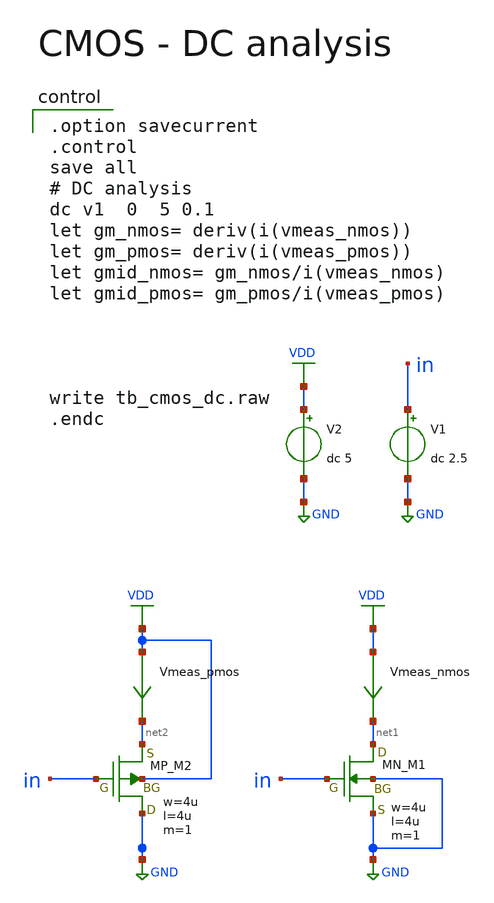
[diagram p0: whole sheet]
** sch_path: member_project/AM_Radio/Yamada3/xschem/tb_cmos_dc.sch
**.subckt tb_cmos_dc
V2 VDD GND dc 5
V1 in GND dc 2.5
XM1 net1 in GND GND NMOS w=4u l=4u as=0 ad=0 ps=0 pd=0 nrd=0 nrs=0 m=1
Vmeas_nmos VDD net1 0
.save i(vmeas_nmos)
Vmeas_pmos VDD net2 0
.save i(vmeas_pmos)
XM2 GND in net2 VDD PMOS w=4u l=4u as=0 ad=0 ps=0 pd=0 nrd=0 nrs=0 m=1
**** begin user architecture code

.option savecurrent
.control
save all
# DC analysis
dc v1  0  5 0.1
let gm_nmos= deriv(i(vmeas_nmos))
let gm_pmos= deriv(i(vmeas_pmos))
let gmid_nmos= gm_nmos/i(vmeas_nmos)
let gmid_pmos= gm_pmos/i(vmeas_pmos)




write tb_cmos_dc.raw
.endc

 .include $::LIB/ip62_models
**** end user architecture code
**.ends
.GLOBAL GND
.GLOBAL VDD
.end
